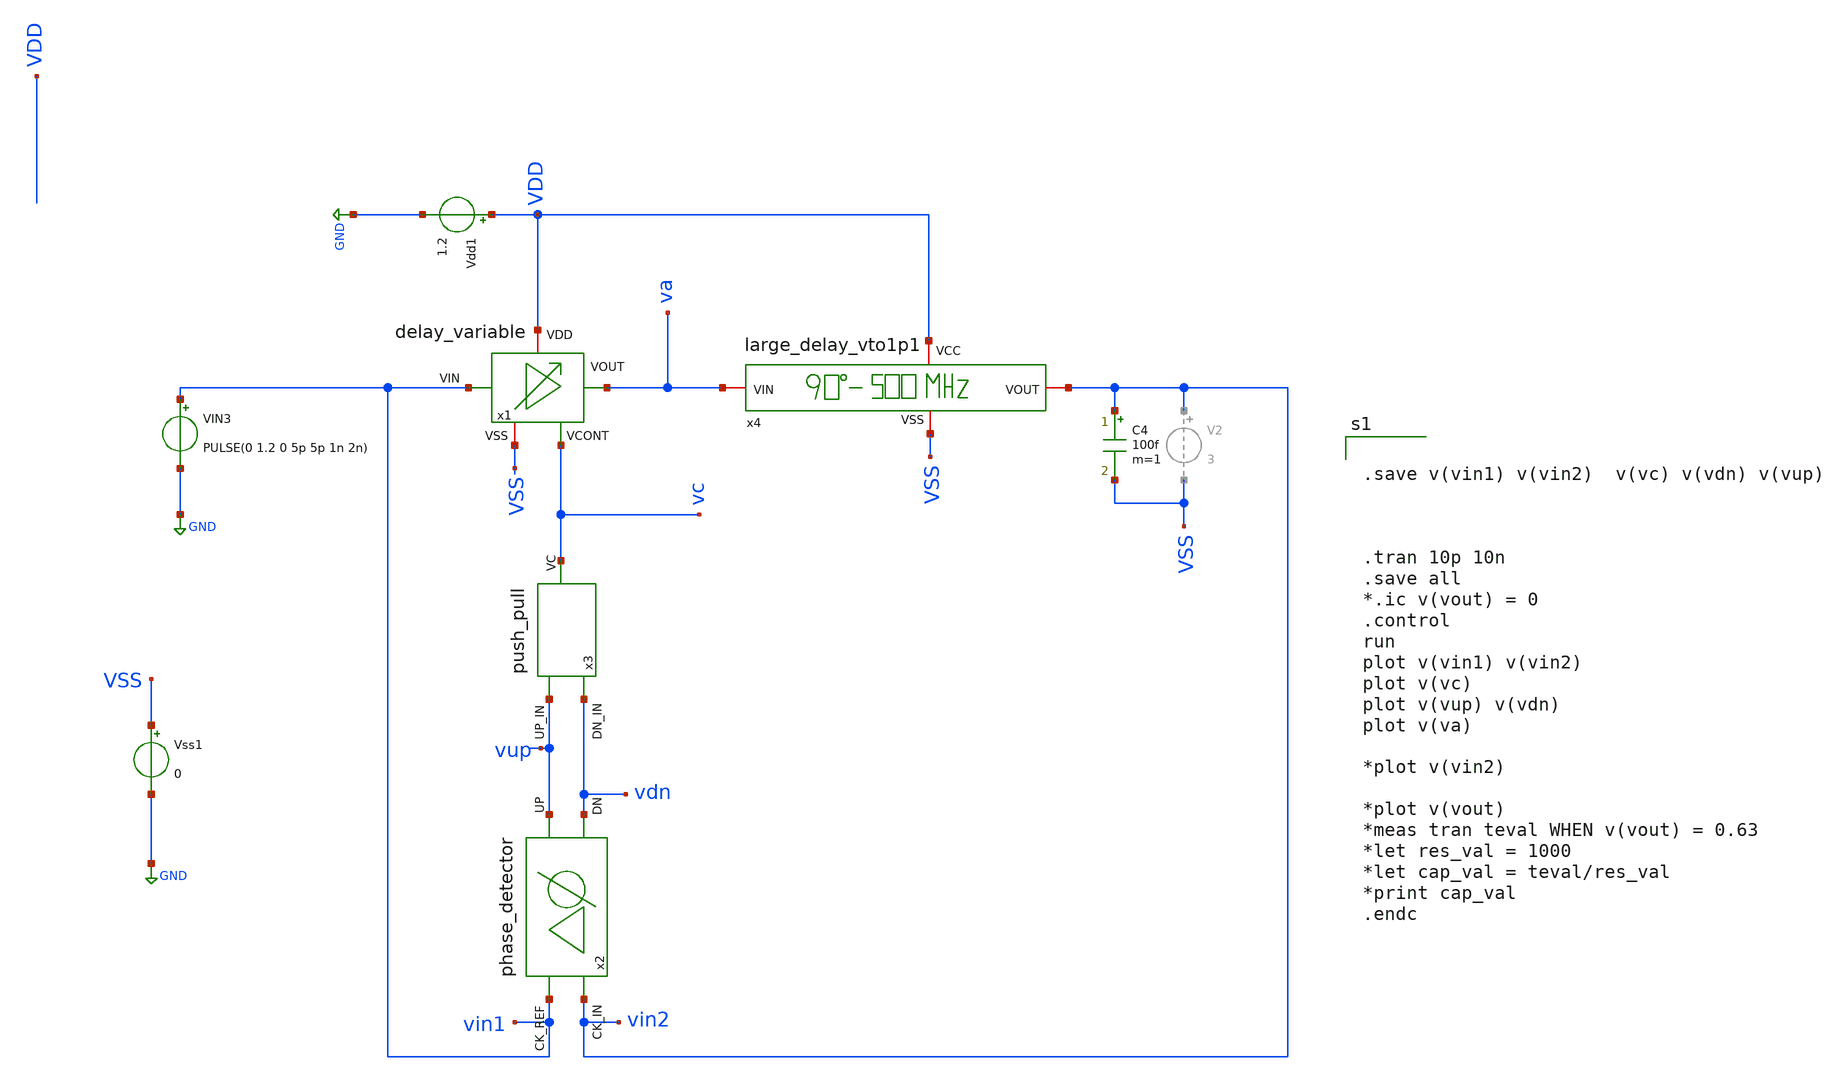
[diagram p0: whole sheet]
** sch_path: sch/DLL/DLL_tb.sch
**.subckt DLL_tb
Vdd1 VDD GND 1.2
C4 vin2 VSS 100f m=1
VIN3 vin1 GND PULSE(0 1.2 0 5p 5p 1n 2n)
Vss1 VSS GND 0
x4 VDD VSS va vin2 large_delay_vto1p1
x1 VDD vin1 va vc VSS delay_variable
x3 vup vc vdn push_pull
x2 vin2 vup vin1 vdn phase_detector
**** begin user architecture code


.save v(vin1) v(vin2)  v(vc) v(vdn) v(vup)



.tran 10p 10n
.save all
*.ic v(vout) = 0
.control
run
plot v(vin1) v(vin2)
plot v(vc)
plot v(vup) v(vdn)
plot v(va)

*plot v(vin2)

*plot v(vout)
*meas tran teval WHEN v(vout) = 0.63
*let res_val = 1000
*let cap_val = teval/res_val
*print cap_val
.endc




.param corner=0

.if (corner==0)
.lib $::SG13G2_MODELS/cornerMOSlv.lib mos_tt
.lib $::SG13G2_MODELS/cornerMOSlv.lib mos_tt
.lib $::SG13G2_MODELS/cornerRES.lib res_typ
.lib $::SG13G2_MODELS/cornerCAP.lib cap_typ
.endif

.include /foss/pdks/ihp-sg13g2/libs.ref/sg13g2_stdcell/spice/sg13g2_stdcell.spice

**** end user architecture code
**.ends
.GLOBAL GND
.end
